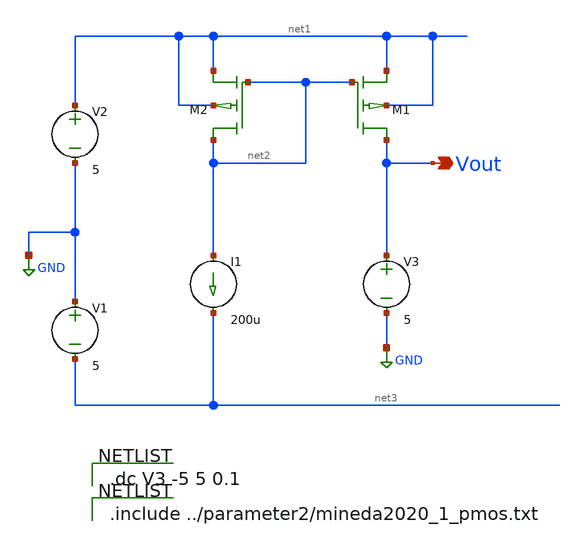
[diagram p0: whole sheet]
** sch_path: currentsource_test14um.sch
**.subckt currentsource_test14um Vout
*.opin Vout
V1 GND net3 5
M1 Vout net2 net1 net1 YSS_PMOS w=14u l=14u as=0 ps=0 ad=0 pd=0 m=1
V2 net1 GND 5
I1 net2 net3 200u
M2 net2 net2 net1 net1 YSS_PMOS w=14u l=14u as=0 ps=0 ad=0 pd=0 m=1
V3 Vout GND 5
**** begin user architecture code

.dc V3 -5 5 0.1


.include ../parameter2/mineda2020_1_pmos.txt

**** end user architecture code
**.ends
.GLOBAL GND
.end
